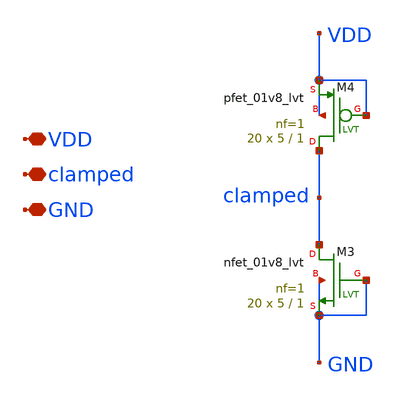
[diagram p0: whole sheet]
** sch_path: xschem/esd.sch
**.subckt esd VDD clamped GND
*.iopin VDD
*.iopin clamped
*.iopin GND
XM3 clamped GND GND GND sky130_fd_pr__nfet_01v8_lvt L=1 W=5 nf=1 ad='int((nf+1)/2) * W/nf * 0.29' as='int((nf+2)/2) * W/nf * 0.29'
+ pd='2*int((nf+1)/2) * (W/nf + 0.29)' ps='2*int((nf+2)/2) * (W/nf + 0.29)' nrd='0.29 / W' nrs='0.29 / W'
+ sa=0 sb=0 sd=0 mult=20 m=20
XM4 clamped VDD VDD VDD sky130_fd_pr__pfet_01v8_lvt L=1 W=5 nf=1 ad='int((nf+1)/2) * W/nf * 0.29' as='int((nf+2)/2) * W/nf * 0.29'
+ pd='2*int((nf+1)/2) * (W/nf + 0.29)' ps='2*int((nf+2)/2) * (W/nf + 0.29)' nrd='0.29 / W' nrs='0.29 / W'
+ sa=0 sb=0 sd=0 mult=20 m=20
**.ends
.end
